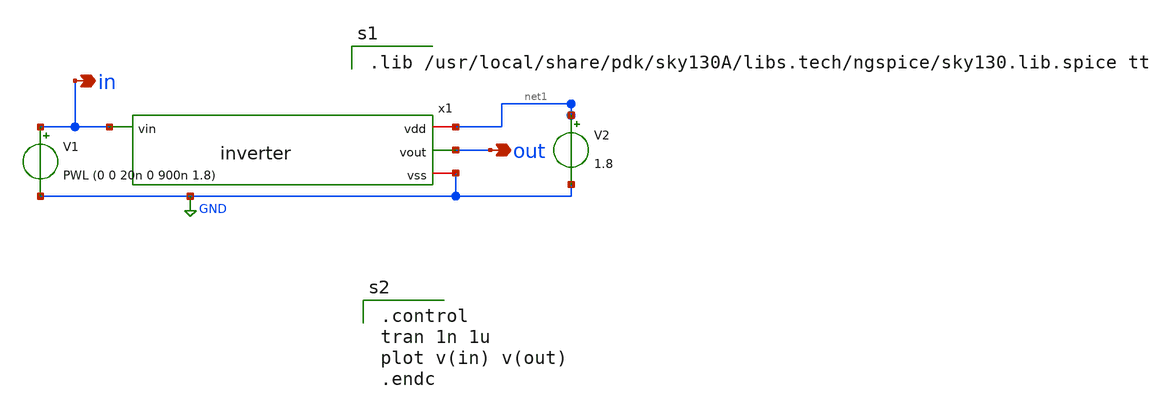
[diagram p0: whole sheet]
** sch_path: ubntu_files/xschem/inverter_tb.sch
**.subckt inverter_tb out in
*.opin out
*.opin in
V1 in GND PWL (0 0 20n 0 900n 1.8)
V2 net1 GND 1.8
x1 net1 out in GND inverter
**** begin user architecture code

.lib /usr/local/share/pdk/sky130A/libs.tech/ngspice/sky130.lib.spice tt


.control
tran 1n 1u
plot v(in) v(out)
.endc

**** end user architecture code
**.ends

* expanding   symbol:  /home/saumya/Desktop/Lab1_and/xschem/inverter.sym # of pins=4
** sym_path: ubntu_files/xschem/inverter.sym
** sch_path: ubntu_files/xschem/inverter.sch
.subckt inverter vdd vout vin vss
*.ipin vin
*.iopin vdd
*.iopin vss
*.opin vout
XM1 vout vin vss vss sky130_fd_pr__nfet_01v8 L=0.18 W=4.5 nf=3 ad= 'int((nf+1)/2) * W/nf * 0.29' as=
+ 'int((nf+2)/2) * W/nf * 0.29' pd= '2*int((nf+1)/2) * (W/nf + 0.29)' ps= '2*int((nf+2)/2) * (W/nf + 0.29)'
+ nrd= '0.29 / W' nrs= '0.29 / W' sa=0 sb=0 sd=0 mult=1 m=1
XM2 vout vin vdd vdd sky130_fd_pr__pfet_01v8 L=0.18 W=3 nf=3 ad= 'int((nf+1)/2) * W/nf * 0.29' as= 'int((nf+2)/2) * W/nf * 0.29'
+ pd= '2*int((nf+1)/2) * (W/nf + 0.29)' ps= '2*int((nf+2)/2) * (W/nf + 0.29)' nrd= '0.29 / W' nrs= '0.29 / W'
+ sa=0 sb=0 sd=0 mult=1 m=1
.ends

.GLOBAL GND
.end
